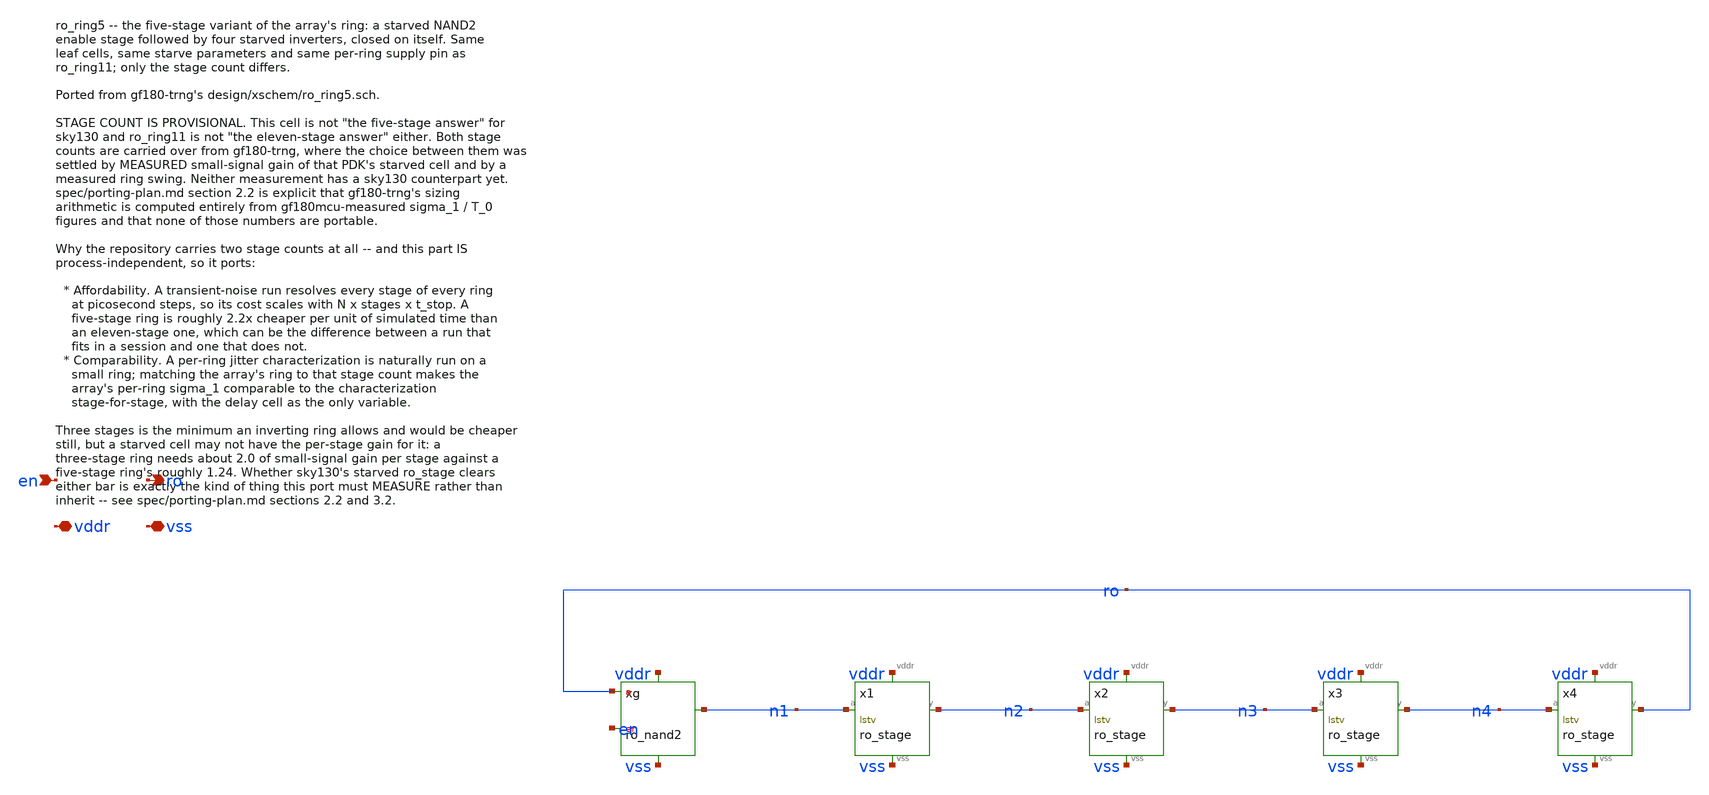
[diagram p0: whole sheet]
** sch_path: design/xschem/ro_ring5.sch
**.subckt ro_ring5 en ro vddr vss
*.ipin en
*.opin ro
*.iopin vddr
*.iopin vss
xg ro en n1 vddr vss ro_nand2 wstv=wstv lstv=lstv cld=cld
x1 n1 n2 vddr vss ro_stage wstv=wstv lstv=lstv cld=cld
x2 n2 n3 vddr vss ro_stage wstv=wstv lstv=lstv cld=cld
x3 n3 n4 vddr vss ro_stage wstv=wstv lstv=lstv cld=cld
x4 n4 ro vddr vss ro_stage wstv=wstv lstv=lstv cld=cld
**.ends

* expanding   symbol:  ro_nand2.sym # of pins=5
** sym_path: design/xschem/ro_nand2.sym
** sch_path: design/xschem/ro_nand2.sch
.subckt ro_nand2 a en y vddr vss  wstv=0.42 lstv=2 cld=0.5f
*.ipin a
*.ipin en
*.opin y
*.iopin vddr
*.iopin vss
XMph py vss vddr vddr sky130_fd_pr__pfet_01v8 L=lstv W=wstv nf=1 ad='int((nf+1)/2) * W/nf * 0.29' as='int((nf+2)/2) * W/nf * 0.29'
+ pd='2*int((nf+1)/2) * (W/nf + 0.29)' ps='2*int((nf+2)/2) * (W/nf + 0.29)' nrd='0.29 / W' nrs='0.29 / W'
+ sa=0 sb=0 sd=0 mult=1 m=1
XMpa y a py vddr sky130_fd_pr__pfet_01v8 L=0.15 W=0.84 nf=1 ad='int((nf+1)/2) * W/nf * 0.29' as='int((nf+2)/2) * W/nf * 0.29'
+ pd='2*int((nf+1)/2) * (W/nf + 0.29)' ps='2*int((nf+2)/2) * (W/nf + 0.29)' nrd='0.29 / W' nrs='0.29 / W'
+ sa=0 sb=0 sd=0 mult=1 m=1
XMpb y en py vddr sky130_fd_pr__pfet_01v8 L=0.15 W=0.84 nf=1 ad='int((nf+1)/2) * W/nf * 0.29' as='int((nf+2)/2) * W/nf * 0.29'
+ pd='2*int((nf+1)/2) * (W/nf + 0.29)' ps='2*int((nf+2)/2) * (W/nf + 0.29)' nrd='0.29 / W' nrs='0.29 / W'
+ sa=0 sb=0 sd=0 mult=1 m=1
XMna y a nm vss sky130_fd_pr__nfet_01v8 L=0.15 W=0.84 nf=1 ad='int((1 + 1)/2) * 0.84 / 1 * 0.29' as='int((1 + 2)/2) * 0.84 / 1 * 0.29'
+ pd='2*int((1 + 1)/2) * (0.84 / 1 + 0.29)' ps='2*int((1 + 2)/2) * (0.84 / 1 + 0.29)' nrd='0.29 / 0.84 '
+ nrs='0.29 / 0.84 ' sa=0 sb=0 sd=0 mult=1 m=1
XMnb nm en ny vss sky130_fd_pr__nfet_01v8 L=0.15 W=0.84 nf=1 ad='int((1 + 1)/2) * 0.84 / 1 * 0.29' as='int((1 + 2)/2) * 0.84 / 1 * 0.29'
+ pd='2*int((1 + 1)/2) * (0.84 / 1 + 0.29)' ps='2*int((1 + 2)/2) * (0.84 / 1 + 0.29)' nrd='0.29 / 0.84 '
+ nrs='0.29 / 0.84 ' sa=0 sb=0 sd=0 mult=1 m=1
XMnt ny vddr vss vss sky130_fd_pr__nfet_01v8 L=lstv W=wstv nf=1 ad='int((1 + 1)/2) * wstv / 1 * 0.29'
+ as='int((1 + 2)/2) * wstv / 1 * 0.29' pd='2*int((1 + 1)/2) * (wstv / 1 + 0.29)' ps='2*int((1 + 2)/2) * (wstv / 1 + 0.29)'
+ nrd='0.29 / wstv ' nrs='0.29 / wstv ' sa=0 sb=0 sd=0 mult=1 m=1
Cld y vss 'cld' m=1
.ends


* expanding   symbol:  ro_stage.sym # of pins=4
** sym_path: design/xschem/ro_stage.sym
** sch_path: design/xschem/ro_stage.sch
.subckt ro_stage a y vddr vss  wstv=0.42 lstv=2 cld=0.5f
*.ipin a
*.opin y
*.iopin vddr
*.iopin vss
XMph py vss vddr vddr sky130_fd_pr__pfet_01v8 L=lstv W=wstv nf=1 ad='int((nf+1)/2) * W/nf * 0.29' as='int((nf+2)/2) * W/nf * 0.29'
+ pd='2*int((nf+1)/2) * (W/nf + 0.29)' ps='2*int((nf+2)/2) * (W/nf + 0.29)' nrd='0.29 / W' nrs='0.29 / W'
+ sa=0 sb=0 sd=0 mult=1 m=1
XMp y a py vddr sky130_fd_pr__pfet_01v8 L=0.15 W=0.84 nf=1 ad='int((nf+1)/2) * W/nf * 0.29' as='int((nf+2)/2) * W/nf * 0.29'
+ pd='2*int((nf+1)/2) * (W/nf + 0.29)' ps='2*int((nf+2)/2) * (W/nf + 0.29)' nrd='0.29 / W' nrs='0.29 / W'
+ sa=0 sb=0 sd=0 mult=1 m=1
XMn y a ny vss sky130_fd_pr__nfet_01v8 L=0.15 W=0.42 nf=1 ad='int((1 + 1)/2) * 0.42 / 1 * 0.29' as='int((1 + 2)/2) * 0.42 / 1 * 0.29'
+ pd='2*int((1 + 1)/2) * (0.42 / 1 + 0.29)' ps='2*int((1 + 2)/2) * (0.42 / 1 + 0.29)' nrd='0.29 / 0.42 '
+ nrs='0.29 / 0.42 ' sa=0 sb=0 sd=0 mult=1 m=1
XMnt ny vddr vss vss sky130_fd_pr__nfet_01v8 L=lstv W=wstv nf=1 ad='int((1 + 1)/2) * wstv / 1 * 0.29'
+ as='int((1 + 2)/2) * wstv / 1 * 0.29' pd='2*int((1 + 1)/2) * (wstv / 1 + 0.29)' ps='2*int((1 + 2)/2) * (wstv / 1 + 0.29)'
+ nrd='0.29 / wstv ' nrs='0.29 / wstv ' sa=0 sb=0 sd=0 mult=1 m=1
Cld y vss 'cld' m=1
.ends

.end
